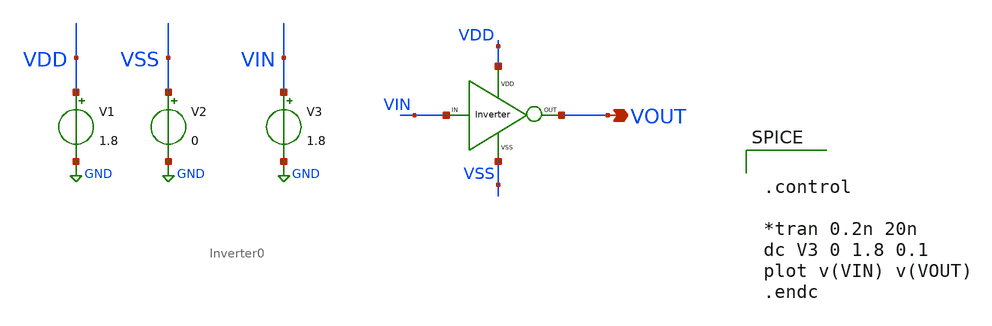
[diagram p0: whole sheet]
** sch_path: xschem/DC_DC_Converter_xschem/DC_DC_Converter/Delay_block_revised/Inverter_0/Inverter0_TB.sch
**.subckt Inverter0_TB VOUT
*.opin VOUT
V1 VDD GND 1.8
V2 VSS GND 0
V3 VIN GND 1.8
X1 VIN VOUT VDD VSS Inverter0
**** begin user architecture code


.control

*tran 0.2n 20n
dc V3 0 1.8 0.1
plot v(VIN) v(VOUT)
.endc



** opencircuitdesign pdks install
.lib $::SKYWATER_MODELS/sky130.lib.spice tt


**** end user architecture code
**.ends

* expanding   symbol:  DC_DC_Converter/Delay_block_revised/Inverter_0/Inverter0.sym # of pins=4
** sym_path: xschem/DC_DC_Converter_xschem/DC_DC_Converter/Delay_block_revised/Inverter_0/Inverter0.sym
** sch_path: xschem/DC_DC_Converter_xschem/DC_DC_Converter/Delay_block_revised/Inverter_0/Inverter0.sch
.subckt Inverter0 VIN VOUT VDD VSS
*.ipin VIN
*.iopin VDD
*.iopin VSS
*.opin VOUT
XM1 VOUT VIN VSS VSS sky130_fd_pr__nfet_01v8 L=0.15 W=0.4 nf=1 ad='int((nf+1)/2) * W/nf * 0.29' as='int((nf+2)/2) * W/nf * 0.29'
+ pd='2*int((nf+1)/2) * (W/nf + 0.29)' ps='2*int((nf+2)/2) * (W/nf + 0.29)' nrd='0.29 / W' nrs='0.29 / W'
+ sa=0 sb=0 sd=0 mult=1 m=1
XM2 VOUT VIN VDD VDD sky130_fd_pr__pfet_01v8 L=0.15 W=1.2 nf=1 ad='int((nf+1)/2) * W/nf * 0.29' as='int((nf+2)/2) * W/nf * 0.29'
+ pd='2*int((nf+1)/2) * (W/nf + 0.29)' ps='2*int((nf+2)/2) * (W/nf + 0.29)' nrd='0.29 / W' nrs='0.29 / W'
+ sa=0 sb=0 sd=0 mult=1 m=1
.ends

.GLOBAL GND
.end
